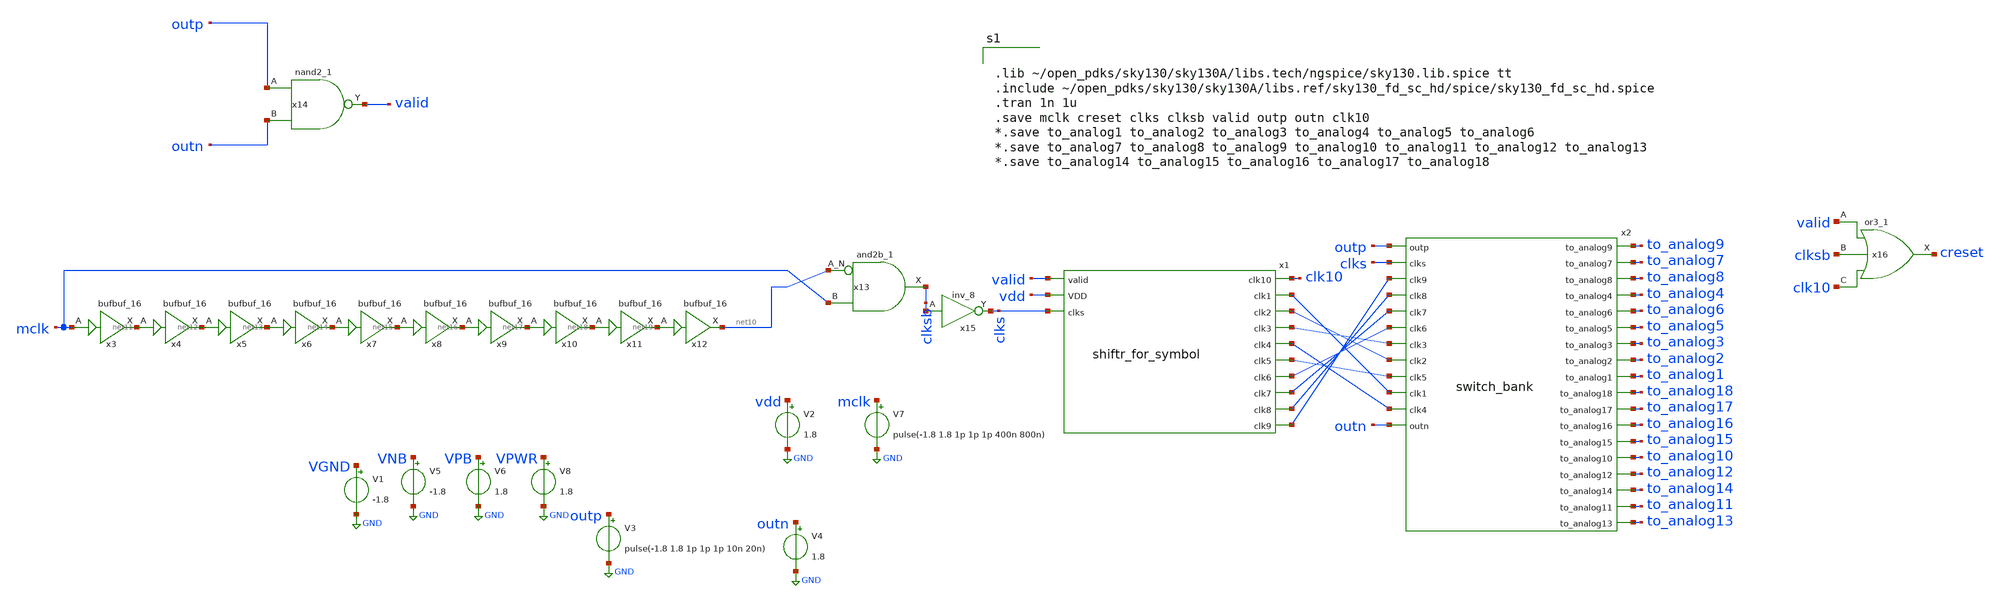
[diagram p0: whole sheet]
** sch_path: d_logic 1.sch
**.subckt d_logic 1
x1 valid clk10 net1 net2 net3 net4 net5 net6 net7 net8 net9 vdd clks shiftr_for_symbol
x2 to_analog9 to_analog7 to_analog8 to_analog4 to_analog6 to_analog5 to_analog3 to_analog2
+ to_analog1 outp clks to_analog18 net9 to_analog17 to_analog16 net8 net7 to_analog15 net6 to_analog10
+ to_analog12 net3 to_analog14 to_analog11 net2 net5 net1 to_analog13 net4 outn switch_bank
V7 mclk GND pulse(-1.8 1.8 1p 1p 1p 400n 800n)
V2 vdd GND 1.8
V3 outp GND pulse(-1.8 1.8 1p 1p 1p 10n 20n)
V4 outn GND 1.8
x3 mclk VGND VNB VPB VPWR net11 sky130_fd_sc_hd__bufbuf_16
x4 net11 VGND VNB VPB VPWR net12 sky130_fd_sc_hd__bufbuf_16
x5 net12 VGND VNB VPB VPWR net13 sky130_fd_sc_hd__bufbuf_16
x6 net13 VGND VNB VPB VPWR net14 sky130_fd_sc_hd__bufbuf_16
x7 net14 VGND VNB VPB VPWR net15 sky130_fd_sc_hd__bufbuf_16
x8 net15 VGND VNB VPB VPWR net16 sky130_fd_sc_hd__bufbuf_16
x9 net16 VGND VNB VPB VPWR net17 sky130_fd_sc_hd__bufbuf_16
x10 net17 VGND VNB VPB VPWR net18 sky130_fd_sc_hd__bufbuf_16
x11 net18 VGND VNB VPB VPWR net19 sky130_fd_sc_hd__bufbuf_16
x12 net19 VGND VNB VPB VPWR net10 sky130_fd_sc_hd__bufbuf_16
x13 net10 mclk VGND VNB VPB VPWR clksb sky130_fd_sc_hd__and2b_1
x14 outp outn VGND VNB VPB VPWR valid sky130_fd_sc_hd__nand2_1
V1 VGND GND -1.8
V5 VNB GND -1.8
V6 VPB GND 1.8
V8 VPWR GND 1.8
x16 valid clksb clk10 VGND VNB VPB VPWR creset sky130_fd_sc_hd__or3_1
x15 clksb VGND VNB VPB VPWR clks sky130_fd_sc_hd__inv_8
**** begin user architecture code


.lib ~/open_pdks/sky130/sky130A/libs.tech/ngspice/sky130.lib.spice tt
.include ~/open_pdks/sky130/sky130A/libs.ref/sky130_fd_sc_hd/spice/sky130_fd_sc_hd.spice
.tran 1n 1u
.save mclk creset clks clksb valid outp outn clk10
*.save to_analog1 to_analog2 to_analog3 to_analog4 to_analog5 to_analog6
*.save to_analog7 to_analog8 to_analog9 to_analog10 to_analog11 to_analog12 to_analog13
*.save to_analog14 to_analog15 to_analog16 to_analog17 to_analog18

**** end user architecture code
**.ends

* expanding   symbol:  /home/cegrahul/Desktop/fyp/shiftr_for_symbol.sym # of pins=13
** sym_path: shiftr_for_symbol.sym
** sch_path: shiftr_for_symbol.sch
.subckt shiftr_for_symbol valid clk10 clk1 clk2 clk3 clk4 clk5 clk6 clk7 clk8 clk9 VDD clks
*.ipin valid
*.ipin VDD
*.ipin clks
*.opin clk1
*.opin clk2
*.opin clk3
*.opin clk4
*.opin clk5
*.opin clk6
*.opin clk7
*.opin clk8
*.opin clk9
*.opin clk10
x1 valid VDD clks VGND VNB VPB VPWR clk1 net1 sky130_fd_sc_hd__dfrbp_2
x2 valid clk1 clks VGND VNB VPB VPWR clk2 net2 sky130_fd_sc_hd__dfrbp_2
x3 valid clk2 clks VGND VNB VPB VPWR clk3 net3 sky130_fd_sc_hd__dfrbp_2
x4 valid clk3 clks VGND VNB VPB VPWR clk4 net4 sky130_fd_sc_hd__dfrbp_2
x5 valid clk4 clks VGND VNB VPB VPWR clk5 net5 sky130_fd_sc_hd__dfrbp_2
x6 valid clk5 clks VGND VNB VPB VPWR clk6 net6 sky130_fd_sc_hd__dfrbp_2
x7 valid clk6 clks VGND VNB VPB VPWR clk7 net7 sky130_fd_sc_hd__dfrbp_2
x8 valid clk7 clks VGND VNB VPB VPWR clk8 net8 sky130_fd_sc_hd__dfrbp_2
x9 valid clk8 clks VGND VNB VPB VPWR clk9 net9 sky130_fd_sc_hd__dfrbp_2
x10 valid clk9 clks VGND VNB VPB VPWR clk10 net10 sky130_fd_sc_hd__dfrbp_2
.ends


* expanding   symbol:  /home/cegrahul/Desktop/fyp/switch_bank.sym # of pins=30
** sym_path: switch_bank.sym
** sch_path: switch_bank.sch
.subckt switch_bank to_analog9 to_analog7 to_analog8 to_analog4 to_analog6 to_analog5 to_analog3
+ to_analog2 to_analog1 outp clks to_analog18 clk9 to_analog17 to_analog16 clk8 clk7 to_analog15 clk6
+ to_analog10 to_analog12 clk3 to_analog14 to_analog11 clk2 clk5 clk1 to_analog13 clk4 outn
*.ipin clk1
*.ipin outp
*.ipin clks
*.ipin outn
*.ipin clk2
*.ipin clk3
*.ipin clk4
*.ipin clk5
*.ipin clk6
*.ipin clk7
*.ipin clk8
*.ipin clk9
*.opin to_analog1
*.opin to_analog2
*.opin to_analog3
*.opin to_analog4
*.opin to_analog5
*.opin to_analog6
*.opin to_analog7
*.opin to_analog8
*.opin to_analog9
*.opin to_analog18
*.opin to_analog17
*.opin to_analog16
*.opin to_analog15
*.opin to_analog14
*.opin to_analog13
*.opin to_analog12
*.opin to_analog11
*.opin to_analog10
x1 clk1 to_analog1 outp clks one_switch_for_symbol
x2 clk2 to_analog2 outp clks one_switch_for_symbol
x3 clk3 to_analog3 outp clks one_switch_for_symbol
x4 clk4 to_analog4 outp clks one_switch_for_symbol
x5 clk5 to_analog5 outp clks one_switch_for_symbol
x6 clk6 to_analog6 outp clks one_switch_for_symbol
x7 clk7 to_analog7 outp clks one_switch_for_symbol
x8 clk8 to_analog8 outp clks one_switch_for_symbol
x9 clk9 to_analog9 outp clks one_switch_for_symbol
x10 clk1 to_analog10 outn clks one_switch_for_symbol
x11 clk2 to_analog11 outn clks one_switch_for_symbol
x12 clk3 to_analog12 outn clks one_switch_for_symbol
x13 clk4 to_analog13 outn clks one_switch_for_symbol
x14 clk5 to_analog14 outn clks one_switch_for_symbol
x15 clk6 to_analog15 outn clks one_switch_for_symbol
x16 clk7 to_analog16 outn clks one_switch_for_symbol
x17 clk8 to_analog17 outn clks one_switch_for_symbol
x18 clk9 to_analog18 outn clks one_switch_for_symbol
.ends


* expanding   symbol:  /home/cegrahul/Desktop/fyp/one_switch_for_symbol.sym # of pins=4
** sym_path: one_switch_for_symbol.sym
** sch_path: one_switch_for_symbol.sch
.subckt one_switch_for_symbol clkx to_analogx outx clks
*.ipin clkx
*.ipin outx
*.ipin clks
*.opin to_analogx
x2 clkx outx clks VGND VNB VPB VPWR net1 net2 sky130_fd_sc_hd__dfrbp_1
x1 clkx net1 VGND VNB VPB VPWR net3 sky130_fd_sc_hd__and2_1
x3 net3 VGND VNB VPB VPWR to_analogx sky130_fd_sc_hd__inv_1
.ends

.GLOBAL GND
.end
